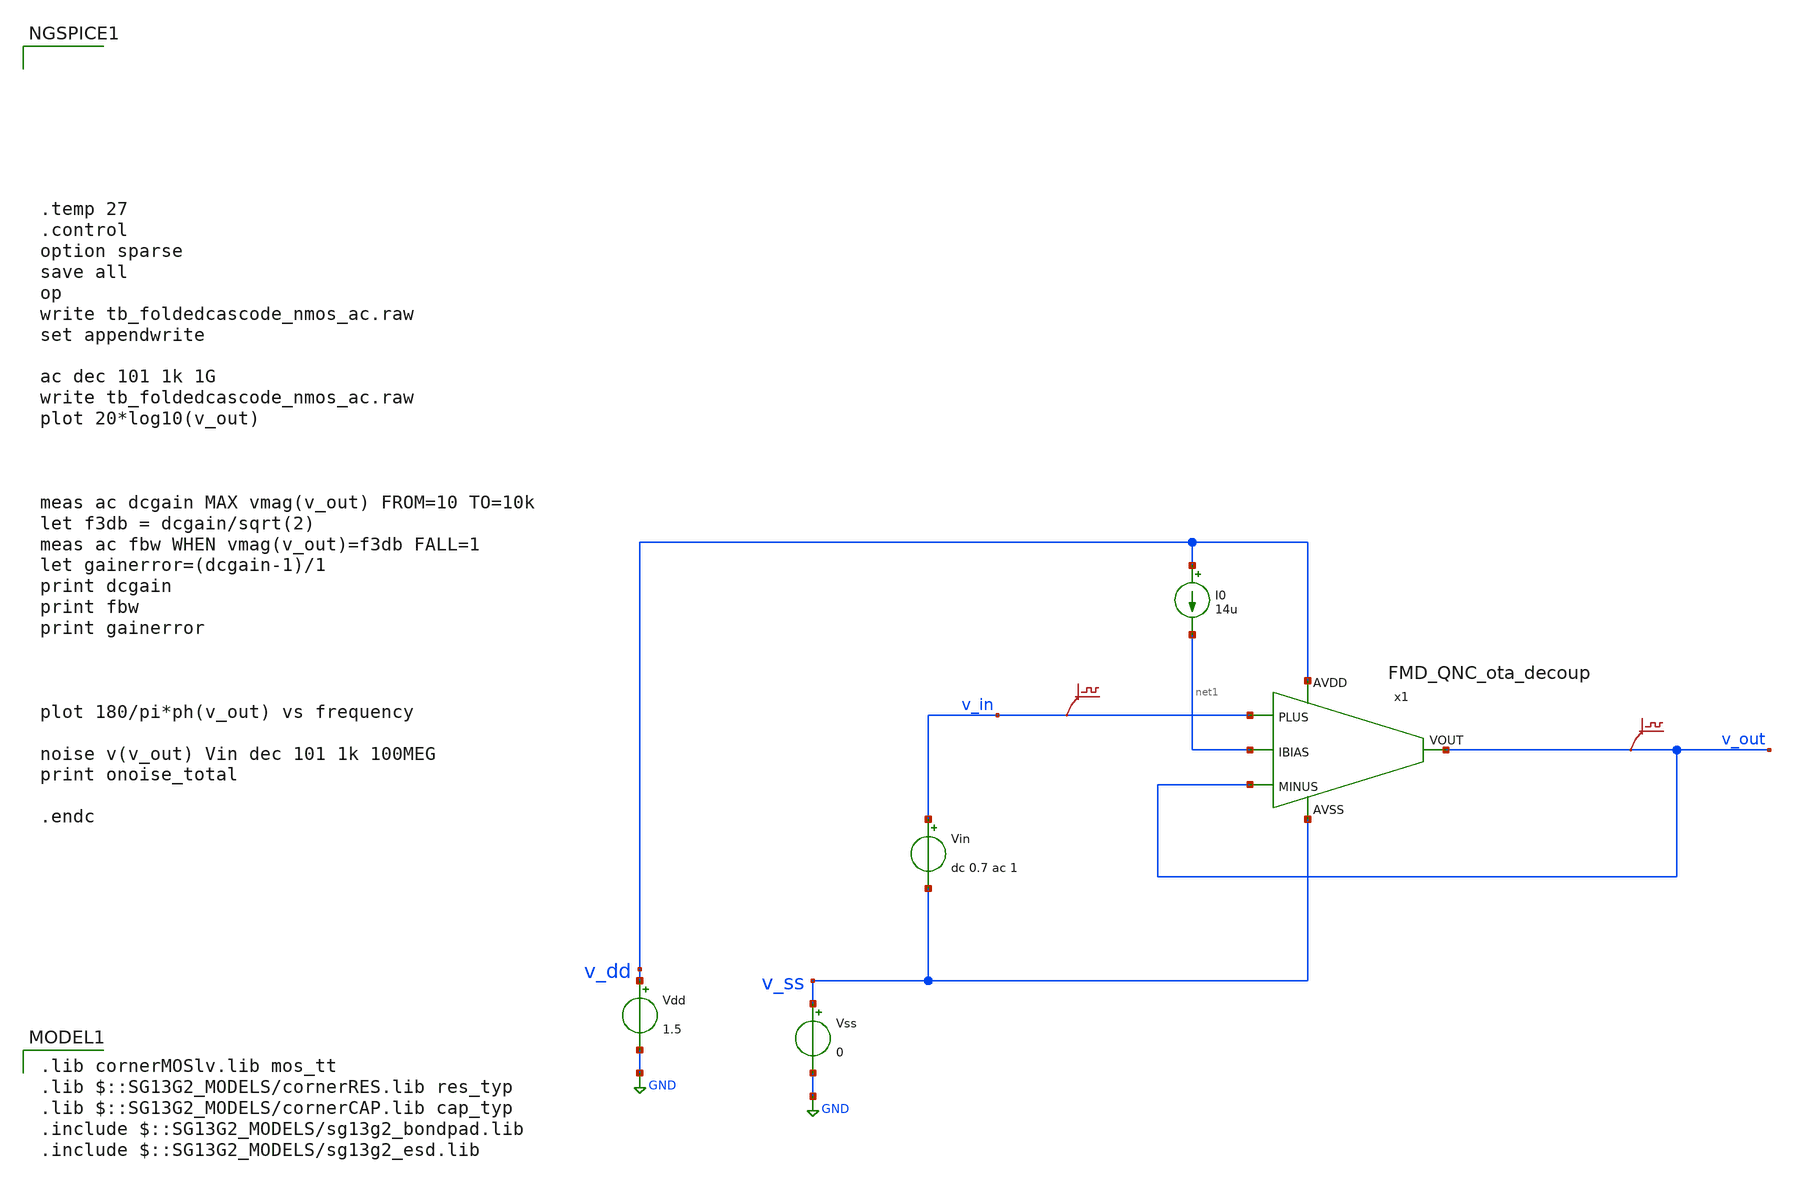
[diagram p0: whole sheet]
** sch_path: ledamp_ph70_b/design_data/xschem/tb_FMD_QNC_ota_decoup_ac.sch
**.subckt tb_FMD_QNC_ota_decoup_ac
Vss v_ss GND 0
Vdd v_dd GND 1.5
Vin v_in v_ss dc 0.7 ac 1
.save v(v_in)
I0 v_dd net1 14u
.save v(v_out)
x1 v_dd net1 v_out v_out v_in v_ss FMD_QNC_ota_decoup
**** begin user architecture code








.temp 27
.control
option sparse
save all
op
write tb_foldedcascode_nmos_ac.raw
set appendwrite

ac dec 101 1k 1G
write tb_foldedcascode_nmos_ac.raw
plot 20*log10(v_out)



meas ac dcgain MAX vmag(v_out) FROM=10 TO=10k
let f3db = dcgain/sqrt(2)
meas ac fbw WHEN vmag(v_out)=f3db FALL=1
let gainerror=(dcgain-1)/1
print dcgain
print fbw
print gainerror



plot 180/pi*ph(v_out) vs frequency

noise v(v_out) Vin dec 101 1k 100MEG
print onoise_total

.endc


 .lib cornerMOSlv.lib mos_tt
.lib $::SG13G2_MODELS/cornerRES.lib res_typ
.lib $::SG13G2_MODELS/cornerCAP.lib cap_typ
.include $::SG13G2_MODELS/sg13g2_bondpad.lib
.include $::SG13G2_MODELS/sg13g2_esd.lib

**** end user architecture code
**.ends
.GLOBAL GND
.end
